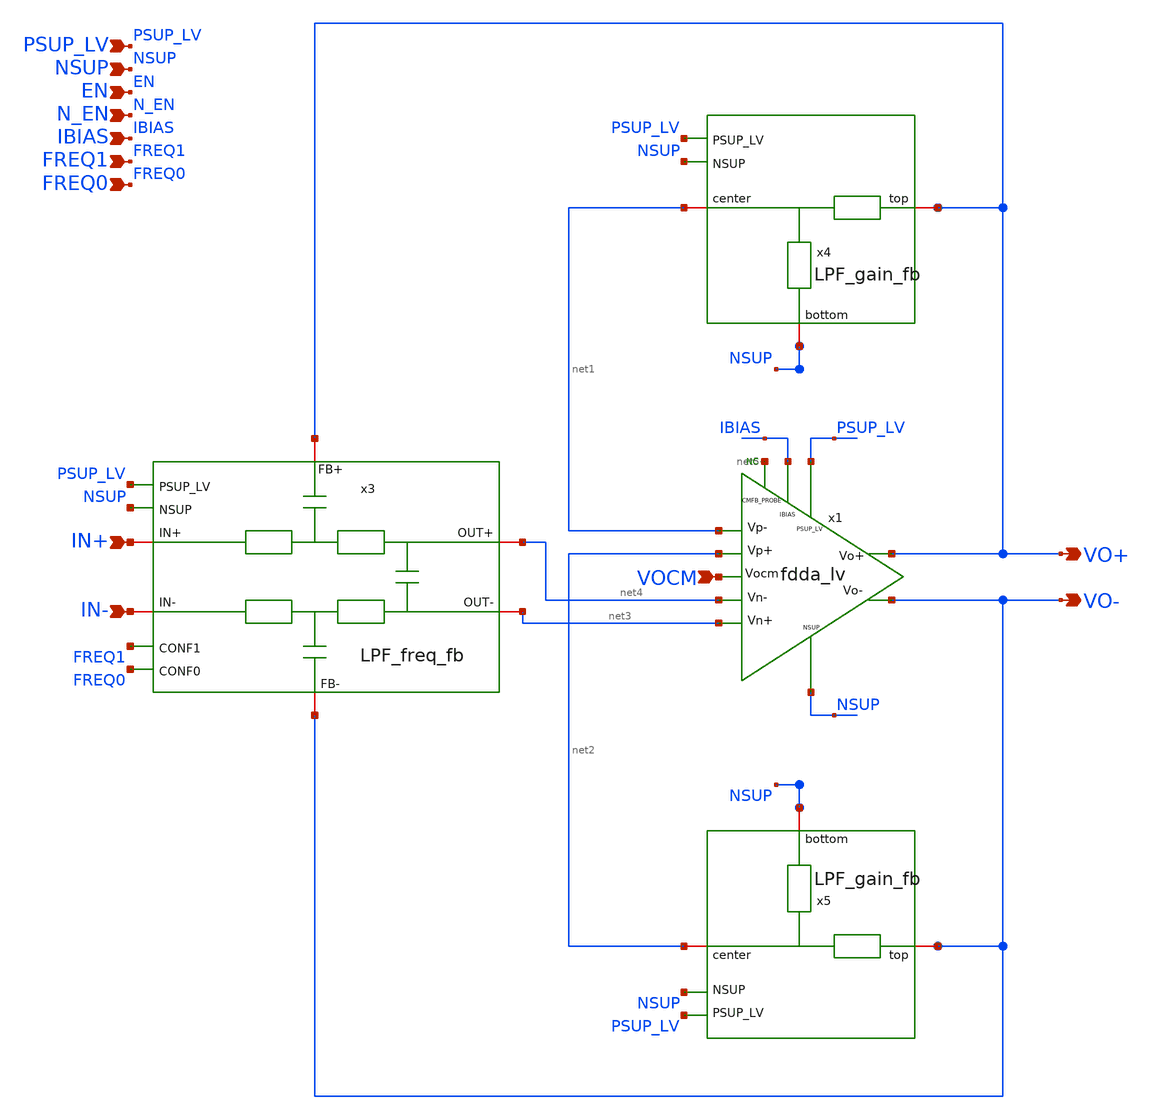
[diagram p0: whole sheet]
** sch_path: xschem/blocks/LPF/LPF.sch
**.subckt LPF NSUP EN N_EN IBIAS PSUP_LV VO+ VO- FREQ1 FREQ0 IN+ IN- VOCM
*.ipin NSUP
*.ipin EN
*.ipin N_EN
*.ipin IBIAS
*.ipin PSUP_LV
*.opin VO+
*.opin VO-
*.ipin FREQ1
*.ipin FREQ0
*.ipin IN+
*.ipin IN-
*.ipin VOCM
* noconn #net5
x1 PSUP_LV net1 net4 net3 net2 VO+ VO- IBIAS NSUP net5 VOCM fdda_lv
x3 VO+ PSUP_LV NSUP net4 IN+ FREQ1 FREQ0 net3 IN- VO- LPF_freq_fb
x4 VO+ net1 PSUP_LV NSUP NSUP LPF_gain_fb
x5 VO- net2 PSUP_LV NSUP NSUP LPF_gain_fb
**.ends
.end
